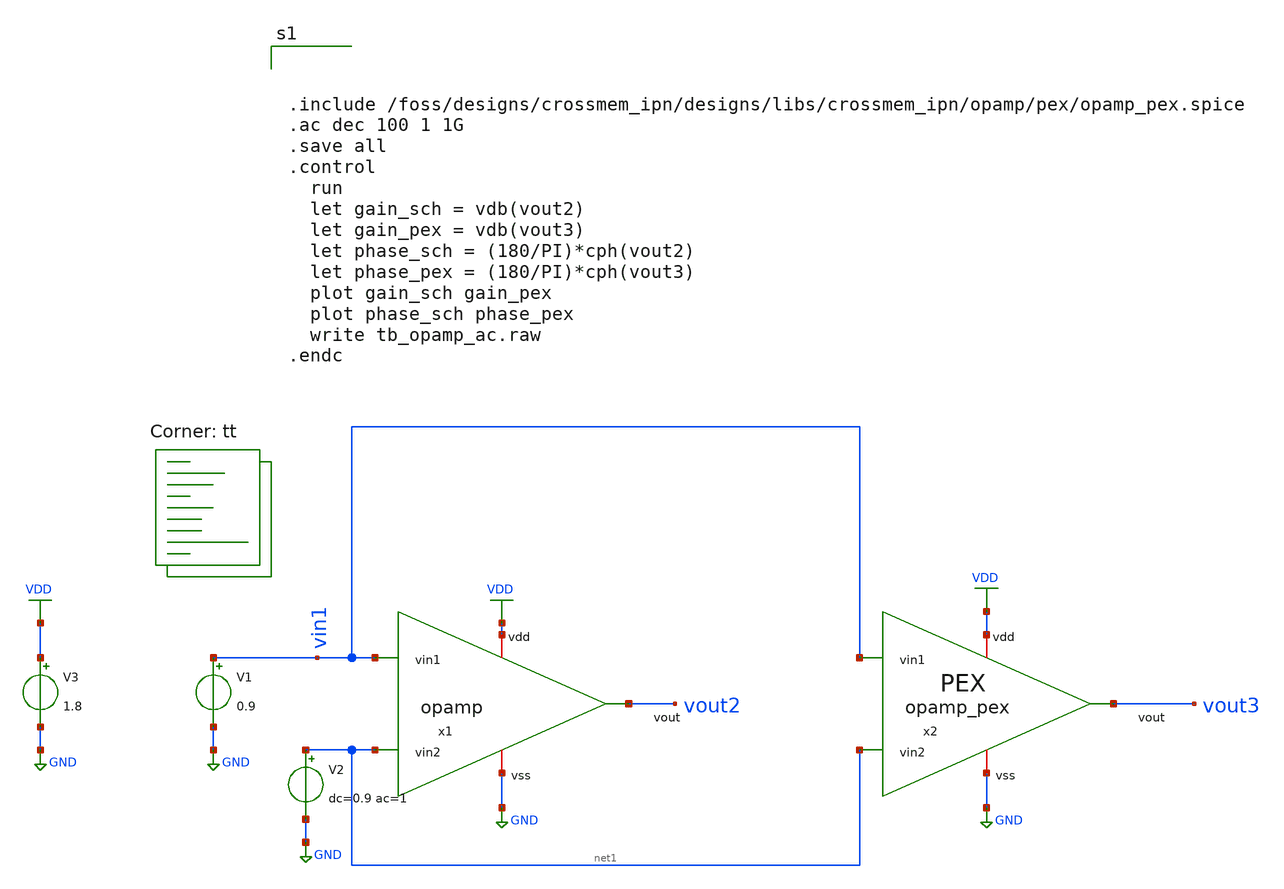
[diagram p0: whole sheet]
** sch_path: designs/libs/crossmem_ipn/opamp/tb_opamp_ac.sch
**.subckt tb_opamp_ac
x1 VDD vin1 net1 vout2 GND opamp
V3 VDD GND 1.8
V2 net1 GND dc=0.9 ac=1
V1 vin1 GND 0.9
x2 VDD GND vin1 net1 vout3 opamp_pex
**** begin user architecture code
.lib $::SKYWATER_MODELS/sky130.lib.spice tt



.include /foss/designs/crossmem_ipn/designs/libs/crossmem_ipn/opamp/pex/opamp_pex.spice
.ac dec 100 1 1G
.save all
.control
  run
  let gain_sch = vdb(vout2)
  let gain_pex = vdb(vout3)
  let phase_sch = (180/PI)*cph(vout2)
  let phase_pex = (180/PI)*cph(vout3)
  plot gain_sch gain_pex
  plot phase_sch phase_pex
  write tb_opamp_ac.raw
.endc


**** end user architecture code
**.ends

* expanding   symbol:  opamp.sym # of pins=5
** sym_path: designs/libs/crossmem_ipn/opamp/opamp.sym
** sch_path: designs/libs/crossmem_ipn/opamp/opamp.sch
.subckt opamp vdd vin1 vin2 vout vss
*.iopin vss
*.iopin vdd
*.opin vout
*.ipin vin1
*.ipin vin2
XM3 net1 net1 vdd vdd sky130_fd_pr__pfet_01v8 L=1 W=9 nf=1 ad='int((1 + 1)/2) * 9 / 1 * 0.29' as='int((1 + 2)/2) * 9 / 1 * 0.29'
+ pd='2*int((1 + 1)/2) * (9 / 1 + 0.29)' ps='2*int((1 + 2)/2) * (9 / 1 + 0.29)' nrd='0.29 / 9 ' nrs='0.29 / 9 '
+ sa=0 sb=0 sd=0 mult=1 m=1
XM4 net2 net1 vdd vdd sky130_fd_pr__pfet_01v8 L=1 W=9 nf=1 ad='int((1 + 1)/2) * 9 / 1 * 0.29' as='int((1 + 2)/2) * 9 / 1 * 0.29'
+ pd='2*int((1 + 1)/2) * (9 / 1 + 0.29)' ps='2*int((1 + 2)/2) * (9 / 1 + 0.29)' nrd='0.29 / 9 ' nrs='0.29 / 9 '
+ sa=0 sb=0 sd=0 mult=1 m=1
XM6 vout net2 vdd vdd sky130_fd_pr__pfet_01v8 L=1 W=8.65 nf=20 ad='int((20 + 1)/2) * 8.65 / 20 * 0.29'
+ as='int((20 + 2)/2) * 8.65 / 20 * 0.29' pd='2*int((20 + 1)/2) * (8.65 / 20 + 0.29)' ps='2*int((20 + 2)/2) * (8.65 / 20 + 0.29)'
+ nrd='0.29 / 8.65 ' nrs='0.29 / 8.65 ' sa=0 sb=0 sd=0 mult=1 m=1
XM1 net1 vin1 net3 vss sky130_fd_pr__nfet_01v8 L=1 W=5 nf=1 ad='int((1 + 1)/2) * 5 / 1 * 0.29' as='int((1 + 2)/2) * 5 / 1 * 0.29'
+ pd='2*int((1 + 1)/2) * (5 / 1 + 0.29)' ps='2*int((1 + 2)/2) * (5 / 1 + 0.29)' nrd='0.29 / 5 ' nrs='0.29 / 5 '
+ sa=0 sb=0 sd=0 mult=1 m=1
XM2 net2 vin2 net3 vss sky130_fd_pr__nfet_01v8 L=1 W=5 nf=1 ad='int((1 + 1)/2) * 5 / 1 * 0.29' as='int((1 + 2)/2) * 5 / 1 * 0.29'
+ pd='2*int((1 + 1)/2) * (5 / 1 + 0.29)' ps='2*int((1 + 2)/2) * (5 / 1 + 0.29)' nrd='0.29 / 5 ' nrs='0.29 / 5 '
+ sa=0 sb=0 sd=0 mult=1 m=1
XM5 net3 vb1 vss vss sky130_fd_pr__nfet_01v8 L=1 W=8 nf=1 ad='int((1 + 1)/2) * 8 / 1 * 0.29' as='int((1 + 2)/2) * 8 / 1 * 0.29'
+ pd='2*int((1 + 1)/2) * (8 / 1 + 0.29)' ps='2*int((1 + 2)/2) * (8 / 1 + 0.29)' nrd='0.29 / 8 ' nrs='0.29 / 8 '
+ sa=0 sb=0 sd=0 mult=1 m=1
XM8 vb1 vb1 vss vss sky130_fd_pr__nfet_01v8 L=1 W=8 nf=1 ad='int((1 + 1)/2) * 8 / 1 * 0.29' as='int((1 + 2)/2) * 8 / 1 * 0.29'
+ pd='2*int((1 + 1)/2) * (8 / 1 + 0.29)' ps='2*int((1 + 2)/2) * (8 / 1 + 0.29)' nrd='0.29 / 8 ' nrs='0.29 / 8 '
+ sa=0 sb=0 sd=0 mult=1 m=1
XM7 vout vb1 vss vss sky130_fd_pr__nfet_01v8 L=1 W=7 nf=16 ad='int((16 + 1)/2) * 7 / 16 * 0.29' as='int((16 + 2)/2) * 7 / 16 * 0.29'
+ pd='2*int((16 + 1)/2) * (7 / 16 + 0.29)' ps='2*int((16 + 2)/2) * (7 / 16 + 0.29)' nrd='0.29 / 7 ' nrs='0.29 / 7 '
+ sa=0 sb=0 sd=0 mult=1 m=1
XC1 net2 vout sky130_fd_pr__cap_mim_m3_1 W=30 L=30 MF=1 m=1
XM9 vb1 vb1 vdd vdd sky130_fd_pr__pfet_01v8 L=0.5 W=0.5 nf=1 ad='int((1 + 1)/2) * 0.5 / 1 * 0.29' as='int((1 + 2)/2) * 0.5 / 1 * 0.29'
+ pd='2*int((1 + 1)/2) * (0.5 / 1 + 0.29)' ps='2*int((1 + 2)/2) * (0.5 / 1 + 0.29)' nrd='0.29 / 0.5 ' nrs='0.29 / 0.5 '
+ sa=0 sb=0 sd=0 mult=1 m=1
.ends

.GLOBAL GND
.GLOBAL VDD
.end
